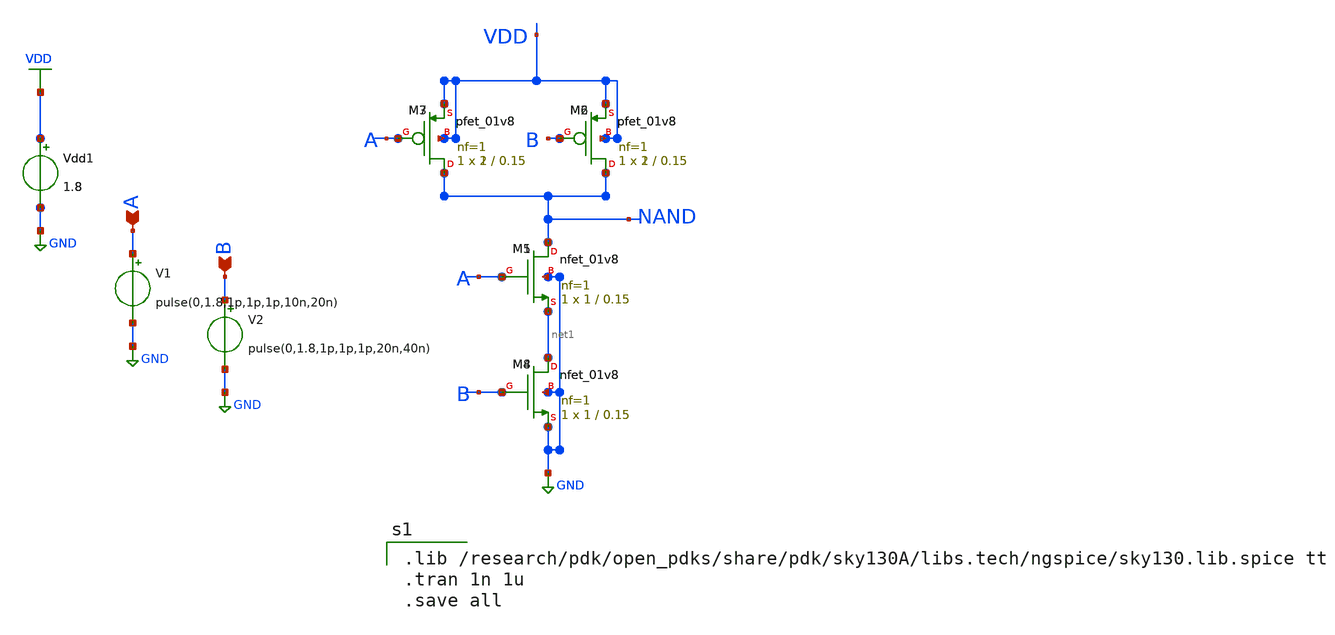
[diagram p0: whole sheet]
** sch_path: skywater_stuff/banana.sch
**.subckt banana A B
*.ipin A
*.ipin B
XM1 NAND A net1 GND sky130_fd_pr__nfet_01v8 L=0.15 W=1 nf=1 ad='int((nf+1)/2) * W/nf * 0.29' as='int((nf+2)/2) * W/nf * 0.29'
+ pd='2*int((nf+1)/2) * (W/nf + 0.29)' ps='2*int((nf+2)/2) * (W/nf + 0.29)' nrd='0.29 / W' nrs='0.29 / W'
+ sa=0 sb=0 sd=0 mult=1 m=1
XM2 NAND B VDD VDD sky130_fd_pr__pfet_01v8 L=0.15 W=2 nf=1 ad='int((nf+1)/2) * W/nf * 0.29' as='int((nf+2)/2) * W/nf * 0.29'
+ pd='2*int((nf+1)/2) * (W/nf + 0.29)' ps='2*int((nf+2)/2) * (W/nf + 0.29)' nrd='0.29 / W' nrs='0.29 / W'
+ sa=0 sb=0 sd=0 mult=1 m=1
XM3 NAND A VDD VDD sky130_fd_pr__pfet_01v8 L=0.15 W=2 nf=1 ad='int((nf+1)/2) * W/nf * 0.29' as='int((nf+2)/2) * W/nf * 0.29'
+ pd='2*int((nf+1)/2) * (W/nf + 0.29)' ps='2*int((nf+2)/2) * (W/nf + 0.29)' nrd='0.29 / W' nrs='0.29 / W'
+ sa=0 sb=0 sd=0 mult=1 m=1
XM4 net1 B GND GND sky130_fd_pr__nfet_01v8 L=0.15 W=1 nf=1 ad='int((nf+1)/2) * W/nf * 0.29' as='int((nf+2)/2) * W/nf * 0.29'
+ pd='2*int((nf+1)/2) * (W/nf + 0.29)' ps='2*int((nf+2)/2) * (W/nf + 0.29)' nrd='0.29 / W' nrs='0.29 / W'
+ sa=0 sb=0 sd=0 mult=1 m=1
Vdd VDD GND 1.8
XM5 NAND A net1 GND sky130_fd_pr__nfet_01v8 L=0.15 W=1 nf=1 ad='int((nf+1)/2) * W/nf * 0.29' as='int((nf+2)/2) * W/nf * 0.29'
+ pd='2*int((nf+1)/2) * (W/nf + 0.29)' ps='2*int((nf+2)/2) * (W/nf + 0.29)' nrd='0.29 / W' nrs='0.29 / W'
+ sa=0 sb=0 sd=0 mult=1 m=1
XM6 NAND B VDD VDD sky130_fd_pr__pfet_01v8 L=0.15 W=1 nf=1 ad='int((nf+1)/2) * W/nf * 0.29' as='int((nf+2)/2) * W/nf * 0.29'
+ pd='2*int((nf+1)/2) * (W/nf + 0.29)' ps='2*int((nf+2)/2) * (W/nf + 0.29)' nrd='0.29 / W' nrs='0.29 / W'
+ sa=0 sb=0 sd=0 mult=1 m=1
XM7 NAND A VDD VDD sky130_fd_pr__pfet_01v8 L=0.15 W=1 nf=1 ad='int((nf+1)/2) * W/nf * 0.29' as='int((nf+2)/2) * W/nf * 0.29'
+ pd='2*int((nf+1)/2) * (W/nf + 0.29)' ps='2*int((nf+2)/2) * (W/nf + 0.29)' nrd='0.29 / W' nrs='0.29 / W'
+ sa=0 sb=0 sd=0 mult=1 m=1
XM8 net1 B GND GND sky130_fd_pr__nfet_01v8 L=0.15 W=1 nf=1 ad='int((nf+1)/2) * W/nf * 0.29' as='int((nf+2)/2) * W/nf * 0.29'
+ pd='2*int((nf+1)/2) * (W/nf + 0.29)' ps='2*int((nf+2)/2) * (W/nf + 0.29)' nrd='0.29 / W' nrs='0.29 / W'
+ sa=0 sb=0 sd=0 mult=1 m=1
Vdd1 VDD GND 1.8
V1 A GND pulse(0,1.8,1p,1p,1p,10n,20n)
V2 B GND pulse(0,1.8,1p,1p,1p,20n,40n)
**** begin user architecture code

.lib /research/pdk/open_pdks/share/pdk/sky130A/libs.tech/ngspice/sky130.lib.spice tt
.tran 1n 1u
.save all

**** end user architecture code
**.ends
.GLOBAL GND
.GLOBAL VDD
.end
